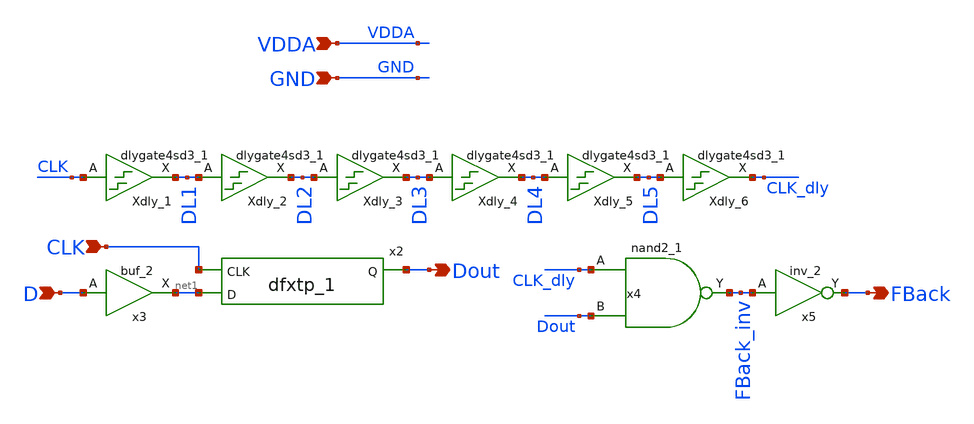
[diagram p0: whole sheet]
** sch_path: xschem/lib/DLib_Quantizer.sch
**.subckt DLib_Quantizer CLK D Dout FBack VDDA GND
*.ipin CLK
*.ipin D
*.opin Dout
*.opin FBack
*.ipin VDDA
*.ipin GND
Xdly_1 CLK GND GND VDDA VDDA DL1 sky130_fd_sc_hd__dlygate4sd3_1
x2 CLK net1 GND GND VDDA VDDA Dout sky130_fd_sc_hd__dfxtp_1
x3 D GND GND VDDA VDDA net1 sky130_fd_sc_hd__buf_2
x4 CLK_dly Dout GND GND VDDA VDDA FBack_inv sky130_fd_sc_hd__nand2_1
x5 FBack_inv GND GND VDDA VDDA FBack sky130_fd_sc_hd__inv_2
Xdly_2 DL1 GND GND VDDA VDDA DL2 sky130_fd_sc_hd__dlygate4sd3_1
Xdly_3 DL2 GND GND VDDA VDDA DL3 sky130_fd_sc_hd__dlygate4sd3_1
Xdly_4 DL3 GND GND VDDA VDDA DL4 sky130_fd_sc_hd__dlygate4sd3_1
Xdly_5 DL4 GND GND VDDA VDDA DL5 sky130_fd_sc_hd__dlygate4sd3_1
Xdly_6 DL5 GND GND VDDA VDDA CLK_dly sky130_fd_sc_hd__dlygate4sd3_1
**.ends
.end
